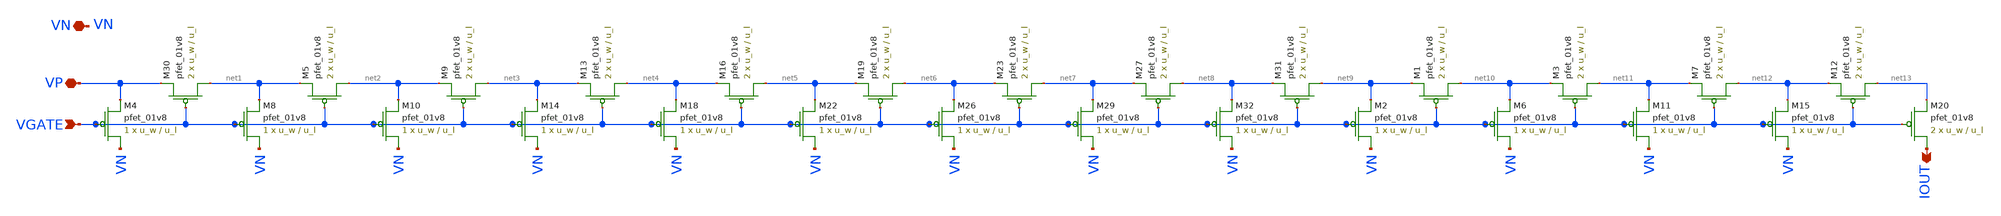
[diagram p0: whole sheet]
** sch_path: lib/analog/schematic/current_divider.sch
**.subckt current_divider VGATE VP VN IOUT
*.ipin VGATE
*.iopin VP
*.iopin VN
*.opin IOUT
XM30 net1 VGATE VP VDD sky130_fd_pr__pfet_01v8 L=u_l W=u_w nf=1 ad='int((nf+1)/2) * W/nf * 0.29' as='int((nf+2)/2) * W/nf * 0.29'
+ pd='2*int((nf+1)/2) * (W/nf + 0.29)' ps='2*int((nf+2)/2) * (W/nf + 0.29)' nrd='0.29 / W' nrs='0.29 / W'
+ sa=0 sb=0 sd=0 mult=2 m=2
XM4 VN VGATE VP VDD sky130_fd_pr__pfet_01v8 L=u_l W=u_w nf=1 ad='int((nf+1)/2) * W/nf * 0.29' as='int((nf+2)/2) * W/nf * 0.29'
+ pd='2*int((nf+1)/2) * (W/nf + 0.29)' ps='2*int((nf+2)/2) * (W/nf + 0.29)' nrd='0.29 / W' nrs='0.29 / W'
+ sa=0 sb=0 sd=0 mult=1 m=1
XM5 net2 VGATE net1 VDD sky130_fd_pr__pfet_01v8 L=u_l W=u_w nf=1 ad='int((nf+1)/2) * W/nf * 0.29' as='int((nf+2)/2) * W/nf * 0.29'
+ pd='2*int((nf+1)/2) * (W/nf + 0.29)' ps='2*int((nf+2)/2) * (W/nf + 0.29)' nrd='0.29 / W' nrs='0.29 / W'
+ sa=0 sb=0 sd=0 mult=2 m=2
XM8 VN VGATE net1 VDD sky130_fd_pr__pfet_01v8 L=u_l W=u_w nf=1 ad='int((nf+1)/2) * W/nf * 0.29' as='int((nf+2)/2) * W/nf * 0.29'
+ pd='2*int((nf+1)/2) * (W/nf + 0.29)' ps='2*int((nf+2)/2) * (W/nf + 0.29)' nrd='0.29 / W' nrs='0.29 / W'
+ sa=0 sb=0 sd=0 mult=1 m=1
XM9 net3 VGATE net2 VDD sky130_fd_pr__pfet_01v8 L=u_l W=u_w nf=1 ad='int((nf+1)/2) * W/nf * 0.29' as='int((nf+2)/2) * W/nf * 0.29'
+ pd='2*int((nf+1)/2) * (W/nf + 0.29)' ps='2*int((nf+2)/2) * (W/nf + 0.29)' nrd='0.29 / W' nrs='0.29 / W'
+ sa=0 sb=0 sd=0 mult=2 m=2
XM10 VN VGATE net2 VDD sky130_fd_pr__pfet_01v8 L=u_l W=u_w nf=1 ad='int((nf+1)/2) * W/nf * 0.29' as='int((nf+2)/2) * W/nf * 0.29'
+ pd='2*int((nf+1)/2) * (W/nf + 0.29)' ps='2*int((nf+2)/2) * (W/nf + 0.29)' nrd='0.29 / W' nrs='0.29 / W'
+ sa=0 sb=0 sd=0 mult=1 m=1
XM13 net4 VGATE net3 VDD sky130_fd_pr__pfet_01v8 L=u_l W=u_w nf=1 ad='int((nf+1)/2) * W/nf * 0.29' as='int((nf+2)/2) * W/nf * 0.29'
+ pd='2*int((nf+1)/2) * (W/nf + 0.29)' ps='2*int((nf+2)/2) * (W/nf + 0.29)' nrd='0.29 / W' nrs='0.29 / W'
+ sa=0 sb=0 sd=0 mult=2 m=2
XM14 VN VGATE net3 VDD sky130_fd_pr__pfet_01v8 L=u_l W=u_w nf=1 ad='int((nf+1)/2) * W/nf * 0.29' as='int((nf+2)/2) * W/nf * 0.29'
+ pd='2*int((nf+1)/2) * (W/nf + 0.29)' ps='2*int((nf+2)/2) * (W/nf + 0.29)' nrd='0.29 / W' nrs='0.29 / W'
+ sa=0 sb=0 sd=0 mult=1 m=1
XM16 net5 VGATE net4 VDD sky130_fd_pr__pfet_01v8 L=u_l W=u_w nf=1 ad='int((nf+1)/2) * W/nf * 0.29' as='int((nf+2)/2) * W/nf * 0.29'
+ pd='2*int((nf+1)/2) * (W/nf + 0.29)' ps='2*int((nf+2)/2) * (W/nf + 0.29)' nrd='0.29 / W' nrs='0.29 / W'
+ sa=0 sb=0 sd=0 mult=2 m=2
XM18 VN VGATE net4 VDD sky130_fd_pr__pfet_01v8 L=u_l W=u_w nf=1 ad='int((nf+1)/2) * W/nf * 0.29' as='int((nf+2)/2) * W/nf * 0.29'
+ pd='2*int((nf+1)/2) * (W/nf + 0.29)' ps='2*int((nf+2)/2) * (W/nf + 0.29)' nrd='0.29 / W' nrs='0.29 / W'
+ sa=0 sb=0 sd=0 mult=1 m=1
XM19 net6 VGATE net5 VDD sky130_fd_pr__pfet_01v8 L=u_l W=u_w nf=1 ad='int((nf+1)/2) * W/nf * 0.29' as='int((nf+2)/2) * W/nf * 0.29'
+ pd='2*int((nf+1)/2) * (W/nf + 0.29)' ps='2*int((nf+2)/2) * (W/nf + 0.29)' nrd='0.29 / W' nrs='0.29 / W'
+ sa=0 sb=0 sd=0 mult=2 m=2
XM22 VN VGATE net5 VDD sky130_fd_pr__pfet_01v8 L=u_l W=u_w nf=1 ad='int((nf+1)/2) * W/nf * 0.29' as='int((nf+2)/2) * W/nf * 0.29'
+ pd='2*int((nf+1)/2) * (W/nf + 0.29)' ps='2*int((nf+2)/2) * (W/nf + 0.29)' nrd='0.29 / W' nrs='0.29 / W'
+ sa=0 sb=0 sd=0 mult=1 m=1
XM23 net7 VGATE net6 VDD sky130_fd_pr__pfet_01v8 L=u_l W=u_w nf=1 ad='int((nf+1)/2) * W/nf * 0.29' as='int((nf+2)/2) * W/nf * 0.29'
+ pd='2*int((nf+1)/2) * (W/nf + 0.29)' ps='2*int((nf+2)/2) * (W/nf + 0.29)' nrd='0.29 / W' nrs='0.29 / W'
+ sa=0 sb=0 sd=0 mult=2 m=2
XM26 VN VGATE net6 VDD sky130_fd_pr__pfet_01v8 L=u_l W=u_w nf=1 ad='int((nf+1)/2) * W/nf * 0.29' as='int((nf+2)/2) * W/nf * 0.29'
+ pd='2*int((nf+1)/2) * (W/nf + 0.29)' ps='2*int((nf+2)/2) * (W/nf + 0.29)' nrd='0.29 / W' nrs='0.29 / W'
+ sa=0 sb=0 sd=0 mult=1 m=1
XM27 net8 VGATE net7 VDD sky130_fd_pr__pfet_01v8 L=u_l W=u_w nf=1 ad='int((nf+1)/2) * W/nf * 0.29' as='int((nf+2)/2) * W/nf * 0.29'
+ pd='2*int((nf+1)/2) * (W/nf + 0.29)' ps='2*int((nf+2)/2) * (W/nf + 0.29)' nrd='0.29 / W' nrs='0.29 / W'
+ sa=0 sb=0 sd=0 mult=2 m=2
XM29 VN VGATE net7 VDD sky130_fd_pr__pfet_01v8 L=u_l W=u_w nf=1 ad='int((nf+1)/2) * W/nf * 0.29' as='int((nf+2)/2) * W/nf * 0.29'
+ pd='2*int((nf+1)/2) * (W/nf + 0.29)' ps='2*int((nf+2)/2) * (W/nf + 0.29)' nrd='0.29 / W' nrs='0.29 / W'
+ sa=0 sb=0 sd=0 mult=1 m=1
XM31 net9 VGATE net8 VDD sky130_fd_pr__pfet_01v8 L=u_l W=u_w nf=1 ad='int((nf+1)/2) * W/nf * 0.29' as='int((nf+2)/2) * W/nf * 0.29'
+ pd='2*int((nf+1)/2) * (W/nf + 0.29)' ps='2*int((nf+2)/2) * (W/nf + 0.29)' nrd='0.29 / W' nrs='0.29 / W'
+ sa=0 sb=0 sd=0 mult=2 m=2
XM32 VN VGATE net8 VDD sky130_fd_pr__pfet_01v8 L=u_l W=u_w nf=1 ad='int((nf+1)/2) * W/nf * 0.29' as='int((nf+2)/2) * W/nf * 0.29'
+ pd='2*int((nf+1)/2) * (W/nf + 0.29)' ps='2*int((nf+2)/2) * (W/nf + 0.29)' nrd='0.29 / W' nrs='0.29 / W'
+ sa=0 sb=0 sd=0 mult=1 m=1
XM1 net10 VGATE net9 VDD sky130_fd_pr__pfet_01v8 L=u_l W=u_w nf=1 ad='int((nf+1)/2) * W/nf * 0.29' as='int((nf+2)/2) * W/nf * 0.29'
+ pd='2*int((nf+1)/2) * (W/nf + 0.29)' ps='2*int((nf+2)/2) * (W/nf + 0.29)' nrd='0.29 / W' nrs='0.29 / W'
+ sa=0 sb=0 sd=0 mult=2 m=2
XM2 VN VGATE net9 VDD sky130_fd_pr__pfet_01v8 L=u_l W=u_w nf=1 ad='int((nf+1)/2) * W/nf * 0.29' as='int((nf+2)/2) * W/nf * 0.29'
+ pd='2*int((nf+1)/2) * (W/nf + 0.29)' ps='2*int((nf+2)/2) * (W/nf + 0.29)' nrd='0.29 / W' nrs='0.29 / W'
+ sa=0 sb=0 sd=0 mult=1 m=1
XM3 net11 VGATE net10 VDD sky130_fd_pr__pfet_01v8 L=u_l W=u_w nf=1 ad='int((nf+1)/2) * W/nf * 0.29' as='int((nf+2)/2) * W/nf * 0.29'
+ pd='2*int((nf+1)/2) * (W/nf + 0.29)' ps='2*int((nf+2)/2) * (W/nf + 0.29)' nrd='0.29 / W' nrs='0.29 / W'
+ sa=0 sb=0 sd=0 mult=2 m=2
XM6 VN VGATE net10 VDD sky130_fd_pr__pfet_01v8 L=u_l W=u_w nf=1 ad='int((nf+1)/2) * W/nf * 0.29' as='int((nf+2)/2) * W/nf * 0.29'
+ pd='2*int((nf+1)/2) * (W/nf + 0.29)' ps='2*int((nf+2)/2) * (W/nf + 0.29)' nrd='0.29 / W' nrs='0.29 / W'
+ sa=0 sb=0 sd=0 mult=1 m=1
XM7 net12 VGATE net11 VDD sky130_fd_pr__pfet_01v8 L=u_l W=u_w nf=1 ad='int((nf+1)/2) * W/nf * 0.29' as='int((nf+2)/2) * W/nf * 0.29'
+ pd='2*int((nf+1)/2) * (W/nf + 0.29)' ps='2*int((nf+2)/2) * (W/nf + 0.29)' nrd='0.29 / W' nrs='0.29 / W'
+ sa=0 sb=0 sd=0 mult=2 m=2
XM11 VN VGATE net11 VDD sky130_fd_pr__pfet_01v8 L=u_l W=u_w nf=1 ad='int((nf+1)/2) * W/nf * 0.29' as='int((nf+2)/2) * W/nf * 0.29'
+ pd='2*int((nf+1)/2) * (W/nf + 0.29)' ps='2*int((nf+2)/2) * (W/nf + 0.29)' nrd='0.29 / W' nrs='0.29 / W'
+ sa=0 sb=0 sd=0 mult=1 m=1
XM12 net13 VGATE net12 VDD sky130_fd_pr__pfet_01v8 L=u_l W=u_w nf=1 ad='int((nf+1)/2) * W/nf * 0.29'
+ as='int((nf+2)/2) * W/nf * 0.29' pd='2*int((nf+1)/2) * (W/nf + 0.29)' ps='2*int((nf+2)/2) * (W/nf + 0.29)'
+ nrd='0.29 / W' nrs='0.29 / W' sa=0 sb=0 sd=0 mult=2 m=2
XM15 VN VGATE net12 VDD sky130_fd_pr__pfet_01v8 L=u_l W=u_w nf=1 ad='int((nf+1)/2) * W/nf * 0.29' as='int((nf+2)/2) * W/nf * 0.29'
+ pd='2*int((nf+1)/2) * (W/nf + 0.29)' ps='2*int((nf+2)/2) * (W/nf + 0.29)' nrd='0.29 / W' nrs='0.29 / W'
+ sa=0 sb=0 sd=0 mult=1 m=1
XM20 IOUT VGATE net13 VDD sky130_fd_pr__pfet_01v8 L=u_l W=u_w nf=1 ad='int((nf+1)/2) * W/nf * 0.29' as='int((nf+2)/2) * W/nf * 0.29'
+ pd='2*int((nf+1)/2) * (W/nf + 0.29)' ps='2*int((nf+2)/2) * (W/nf + 0.29)' nrd='0.29 / W' nrs='0.29 / W'
+ sa=0 sb=0 sd=0 mult=2 m=2
**.ends
.end
